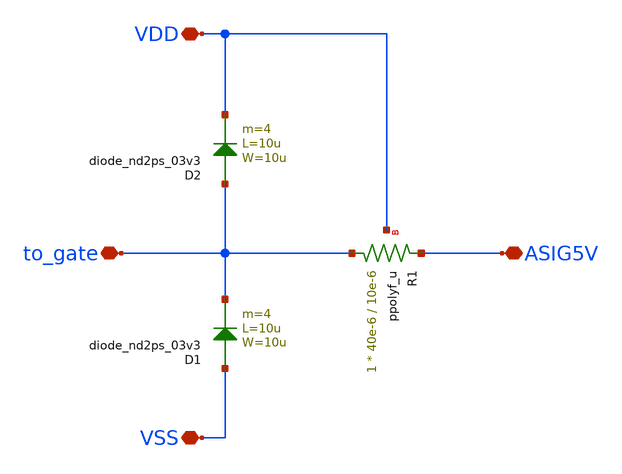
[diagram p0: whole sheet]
** sch_path: designs/libs/A5_core/A5_top/cmd_esd_prot/cmd_esd_prot.sch
**.subckt cmd_esd_prot VDD to_gate VSS ASIG5V
*.iopin VDD
*.iopin to_gate
*.iopin VSS
*.iopin ASIG5V
XR1 to_gate ASIG5V VDD ppolyf_u r_width=40e-6 r_length=10e-6 m=1
D1 VSS to_gate diode_nd2ps_03v3 area='10u * 10u ' pj='2*10u + 2*10u ' m=4
D2 to_gate VDD diode_nd2ps_03v3 area='10u * 10u ' pj='2*10u + 2*10u ' m=4
**.ends
.end
